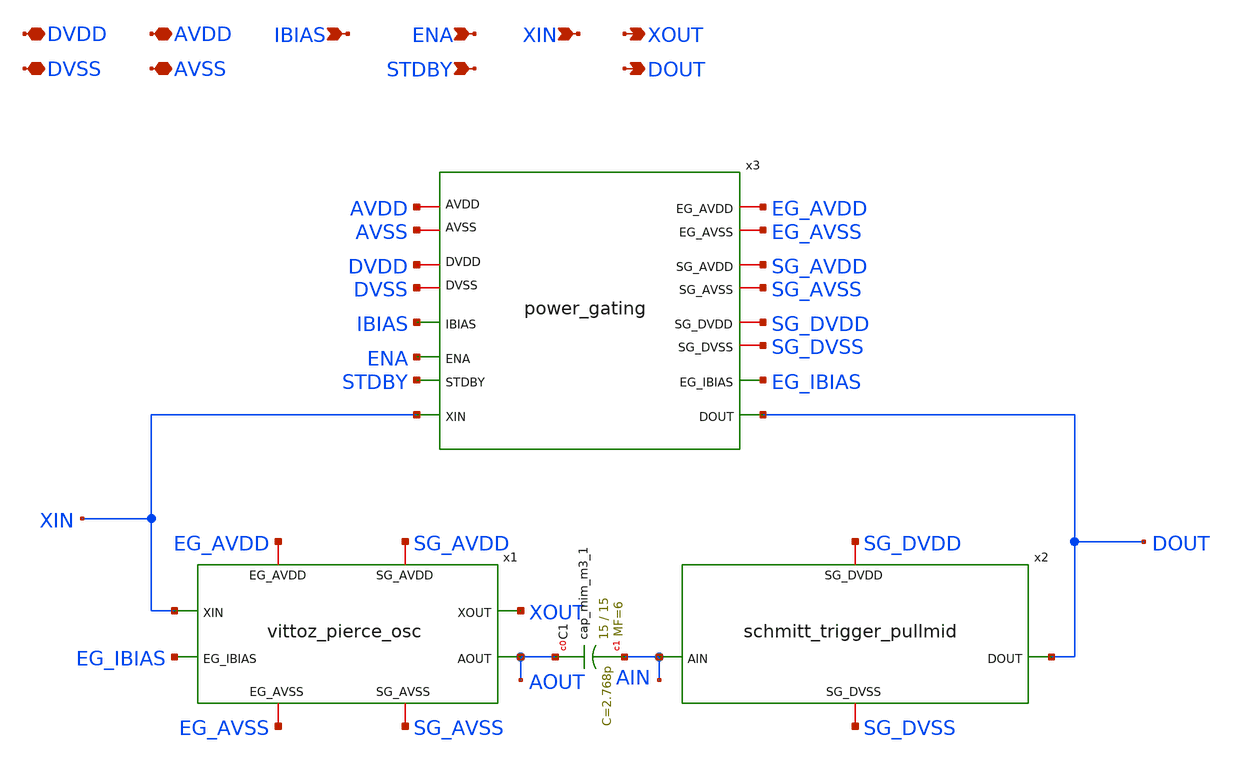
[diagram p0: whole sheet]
** sch_path: xschem/sky130_ht_ip__hsxo_cpz1.sch
**.subckt sky130_ht_ip__hsxo_cpz1 DVDD DVSS AVDD AVSS ENA STDBY XIN XOUT DOUT IBIAS
*.iopin DVDD
*.iopin DVSS
*.iopin AVDD
*.iopin AVSS
*.ipin ENA
*.ipin STDBY
*.ipin XIN
*.opin XOUT
*.opin DOUT
*.ipin IBIAS
x1 XOUT SG_AVDD EG_AVDD XIN EG_IBIAS AOUT SG_AVSS EG_AVSS vittoz_pierce_osc
x2 SG_DVDD AIN DOUT SG_DVSS schmitt_trigger_pullmid
XC1 AOUT AIN sky130_fd_pr__cap_mim_m3_1 W=15 L=15 MF=6 m=6
x3 DOUT SG_AVDD DVDD EG_IBIAS SG_DVDD AVDD IBIAS EG_AVDD ENA SG_DVSS SG_AVSS STDBY EG_AVSS AVSS DVSS
+ XIN power_gating
**.ends

* expanding   symbol:  vittoz_pierce_osc.sym # of pins=8
** sym_path: xschem/vittoz_pierce_osc.sym
** sch_path: xschem/vittoz_pierce_osc.sch
.subckt vittoz_pierce_osc XOUT SG_AVDD EG_AVDD XIN EG_IBIAS AOUT SG_AVSS EG_AVSS
*.iopin EG_AVDD
*.iopin EG_AVSS
*.iopin SG_AVDD
*.iopin SG_AVSS
*.ipin XIN
*.ipin EG_IBIAS
*.opin XOUT
*.opin AOUT
XM9 net6 PBIAS EG_AVDD EG_AVDD sky130_fd_pr__pfet_g5v0d10v5 L=0.5 W=1024 nf=32 ad='int((nf+1)/2) * W/nf * 0.29'
+ as='int((nf+2)/2) * W/nf * 0.29' pd='2*int((nf+1)/2) * (W/nf + 0.29)' ps='2*int((nf+2)/2) * (W/nf + 0.29)'
+ nrd='0.29 / W' nrs='0.29 / W' sa=0 sb=0 sd=0 mult=1 m=1
XM10 net7 PBIAS EG_AVDD EG_AVDD sky130_fd_pr__pfet_g5v0d10v5 L=0.5 W=128 nf=4 ad='int((nf+1)/2) * W/nf * 0.29'
+ as='int((nf+2)/2) * W/nf * 0.29' pd='2*int((nf+1)/2) * (W/nf + 0.29)' ps='2*int((nf+2)/2) * (W/nf + 0.29)'
+ nrd='0.29 / W' nrs='0.29 / W' sa=0 sb=0 sd=0 mult=1 m=1
XM11 PBIAS PBIAS EG_AVDD EG_AVDD sky130_fd_pr__pfet_g5v0d10v5 L=0.5 W=128 nf=4 ad='int((nf+1)/2) * W/nf * 0.29'
+ as='int((nf+2)/2) * W/nf * 0.29' pd='2*int((nf+1)/2) * (W/nf + 0.29)' ps='2*int((nf+2)/2) * (W/nf + 0.29)'
+ nrd='0.29 / W' nrs='0.29 / W' sa=0 sb=0 sd=0 mult=1 m=1
Vmeas3 net6 XOUT 0
.save i(vmeas3)
Vmeas4 net7 net1 0
.save i(vmeas4)
Vmeas2 PBIAS net3 0
.save i(vmeas2)
XM12 net1 net2 EG_AVSS EG_AVSS sky130_fd_pr__nfet_g5v0d10v5 L=0.5 W=128 nf=4 ad='int((nf+1)/2) * W/nf * 0.29'
+ as='int((nf+2)/2) * W/nf * 0.29' pd='2*int((nf+1)/2) * (W/nf + 0.29)' ps='2*int((nf+2)/2) * (W/nf + 0.29)'
+ nrd='0.29 / W' nrs='0.29 / W' sa=0 sb=0 sd=0 mult=1 m=1
XR1 net2 net1 EG_AVSS sky130_fd_pr__res_xhigh_po_0p35 L=7 mult=1 m=1
XC1 net1 EG_AVSS sky130_fd_pr__cap_mim_m3_1 W=2 L=2 MF=1 m=1
XC2 XIN net2 sky130_fd_pr__cap_mim_m3_1 W=15 L=15 MF=6 m=6
XC7 net2 EG_AVSS sky130_fd_pr__cap_mim_m3_1 W=15 L=15 MF=6 m=6
XM13 XOUT XIN EG_AVSS EG_AVSS sky130_fd_pr__nfet_g5v0d10v5 L=0.5 W=32 nf=8 ad='int((nf+1)/2) * W/nf * 0.29'
+ as='int((nf+2)/2) * W/nf * 0.29' pd='2*int((nf+1)/2) * (W/nf + 0.29)' ps='2*int((nf+2)/2) * (W/nf + 0.29)'
+ nrd='0.29 / W' nrs='0.29 / W' sa=0 sb=0 sd=0 mult=1 m=1
XM14 net3 net2 net5 EG_AVSS sky130_fd_pr__nfet_g5v0d10v5 L=0.5 W=1024 nf=32 ad='int((nf+1)/2) * W/nf * 0.29'
+ as='int((nf+2)/2) * W/nf * 0.29' pd='2*int((nf+1)/2) * (W/nf + 0.29)' ps='2*int((nf+2)/2) * (W/nf + 0.29)'
+ nrd='0.29 / W' nrs='0.29 / W' sa=0 sb=0 sd=0 mult=1 m=1
XM15 net5 net4 EG_AVSS EG_AVSS sky130_fd_pr__nfet_g5v0d10v5 L=0.5 W=128 nf=4 ad='int((nf+1)/2) * W/nf * 0.29'
+ as='int((nf+2)/2) * W/nf * 0.29' pd='2*int((nf+1)/2) * (W/nf + 0.29)' ps='2*int((nf+2)/2) * (W/nf + 0.29)'
+ nrd='0.29 / W' nrs='0.29 / W' sa=0 sb=0 sd=0 mult=1 m=1
XM16 net4 net4 EG_AVSS EG_AVSS sky130_fd_pr__nfet_g5v0d10v5 L=0.5 W=8 nf=1 ad='int((nf+1)/2) * W/nf * 0.29'
+ as='int((nf+2)/2) * W/nf * 0.29' pd='2*int((nf+1)/2) * (W/nf + 0.29)' ps='2*int((nf+2)/2) * (W/nf + 0.29)'
+ nrd='0.29 / W' nrs='0.29 / W' sa=0 sb=0 sd=0 mult=1 m=1
XR3 XIN XOUT EG_AVSS sky130_fd_pr__res_xhigh_po_0p35 L=2.8 mult=1 m=1
XM17 AOUT XIN SG_AVSS SG_AVSS sky130_fd_pr__nfet_g5v0d10v5 L=0.5 W=4 nf=1 ad='int((nf+1)/2) * W/nf * 0.29'
+ as='int((nf+2)/2) * W/nf * 0.29' pd='2*int((nf+1)/2) * (W/nf + 0.29)' ps='2*int((nf+2)/2) * (W/nf + 0.29)'
+ nrd='0.29 / W' nrs='0.29 / W' sa=0 sb=0 sd=0 mult=1 m=1
XM18 net8 PBIAS SG_AVDD SG_AVDD sky130_fd_pr__pfet_g5v0d10v5 L=0.5 W=128 nf=4 ad='int((nf+1)/2) * W/nf * 0.29'
+ as='int((nf+2)/2) * W/nf * 0.29' pd='2*int((nf+1)/2) * (W/nf + 0.29)' ps='2*int((nf+2)/2) * (W/nf + 0.29)'
+ nrd='0.29 / W' nrs='0.29 / W' sa=0 sb=0 sd=0 mult=1 m=1
Vmeas5 net8 AOUT 0
.save i(vmeas5)
XC8 AOUT SG_AVSS sky130_fd_pr__cap_mim_m3_1 W=2 L=2 MF=1 m=1
XC3 EG_AVDD EG_AVSS sky130_fd_pr__cap_mim_m3_1 W=15 L=15 MF=6 m=6
XC4 SG_AVDD SG_AVSS sky130_fd_pr__cap_mim_m3_1 W=15 L=15 MF=6 m=6
Vmeas1 EG_IBIAS net4 0
.save i(vmeas1)
.ends


* expanding   symbol:  schmitt_trigger_pullmid.sym # of pins=4
** sym_path: xschem/schmitt_trigger_pullmid.sym
** sch_path: xschem/schmitt_trigger_pullmid.sch
.subckt schmitt_trigger_pullmid SG_DVDD AIN DOUT SG_DVSS
*.iopin SG_DVDD
*.iopin SG_DVSS
*.ipin AIN
*.opin DOUT
XR3 net2 net1 SG_DVSS sky130_fd_pr__res_xhigh_po_0p35 L=128 mult=1 m=1
XM3 DOUT net2 DHT SG_DVDD sky130_fd_pr__pfet_01v8 L=0.3 W=1 nf=1 ad='int((1 + 1)/2) * 1 / 1 * 0.29' as='int((1 + 2)/2) * 1 / 1 * 0.29'
+ pd='2*int((1 + 1)/2) * (1 / 1 + 0.29)' ps='2*int((1 + 2)/2) * (1 / 1 + 0.29)' nrd='0.29 / 1 ' nrs='0.29 / 1 '
+ sa=0 sb=0 sd=0 mult=1 m=1
XM4 DOUT net2 DLT SG_DVSS sky130_fd_pr__nfet_01v8 L=0.2 W=1 nf=1 ad='int((nf+1)/2) * W/nf * 0.29' as='int((nf+2)/2) * W/nf * 0.29'
+ pd='2*int((nf+1)/2) * (W/nf + 0.29)' ps='2*int((nf+2)/2) * (W/nf + 0.29)' nrd='0.29 / W' nrs='0.29 / W'
+ sa=0 sb=0 sd=0 mult=1 m=1
XM5 DHT net2 SG_DVDD SG_DVDD sky130_fd_pr__pfet_01v8 L=0.3 W=1 nf=1 ad='int((1 + 1)/2) * 1 / 1 * 0.29'
+ as='int((1 + 2)/2) * 1 / 1 * 0.29' pd='2*int((1 + 1)/2) * (1 / 1 + 0.29)' ps='2*int((1 + 2)/2) * (1 / 1 + 0.29)'
+ nrd='0.29 / 1 ' nrs='0.29 / 1 ' sa=0 sb=0 sd=0 mult=1 m=1
XM6 DLT net2 SG_DVSS SG_DVSS sky130_fd_pr__nfet_01v8 L=0.2 W=1 nf=1 ad='int((nf+1)/2) * W/nf * 0.29'
+ as='int((nf+2)/2) * W/nf * 0.29' pd='2*int((nf+1)/2) * (W/nf + 0.29)' ps='2*int((nf+2)/2) * (W/nf + 0.29)'
+ nrd='0.29 / W' nrs='0.29 / W' sa=0 sb=0 sd=0 mult=1 m=1
XM7 SG_DVSS DOUT DHT SG_DVDD sky130_fd_pr__pfet_01v8 L=0.3 W=1 nf=1 ad='int((1 + 1)/2) * 1 / 1 * 0.29'
+ as='int((1 + 2)/2) * 1 / 1 * 0.29' pd='2*int((1 + 1)/2) * (1 / 1 + 0.29)' ps='2*int((1 + 2)/2) * (1 / 1 + 0.29)'
+ nrd='0.29 / 1 ' nrs='0.29 / 1 ' sa=0 sb=0 sd=0 mult=1 m=1
XM8 SG_DVDD DOUT DLT SG_DVSS sky130_fd_pr__nfet_01v8 L=0.2 W=1 nf=1 ad='int((nf+1)/2) * W/nf * 0.29'
+ as='int((nf+2)/2) * W/nf * 0.29' pd='2*int((nf+1)/2) * (W/nf + 0.29)' ps='2*int((nf+2)/2) * (W/nf + 0.29)'
+ nrd='0.29 / W' nrs='0.29 / W' sa=0 sb=0 sd=0 mult=1 m=1
XC4 SG_DVDD SG_DVSS sky130_fd_pr__cap_mim_m3_1 W=15 L=15 MF=6 m=6
XR1 net1 SG_DVDD SG_DVSS sky130_fd_pr__res_xhigh_po_0p35 L=16 mult=1 m=1
XR2 SG_DVSS net1 SG_DVSS sky130_fd_pr__res_xhigh_po_0p35 L=16 mult=1 m=1
Vmeas6 AIN net2 0
.save i(vmeas6)
.ends


* expanding   symbol:  /foss/designs/hsxo-cpz1/xschem/power_gating.sym # of pins=16
** sym_path: xschem/power_gating.sym
** sch_path: xschem/power_gating.sch
.subckt power_gating DOUT SG_AVDD DVDD EG_IBIAS SG_DVDD AVDD IBIAS EG_AVDD ENA SG_DVSS SG_AVSS STDBY
+ EG_AVSS AVSS DVSS XIN
*.iopin DVDD
*.iopin DVSS
*.iopin AVDD
*.iopin AVSS
*.ipin ENA
*.ipin STDBY
*.opin DOUT
*.ipin IBIAS
*.iopin EG_AVDD
*.iopin EG_AVSS
*.iopin SG_AVDD
*.iopin SG_AVSS
*.iopin SG_DVDD
*.iopin SG_DVSS
*.opin EG_IBIAS
*.ipin XIN
x3 AVDD ENA_B DVDD ENA ENA_H AVSS DVSS ENA_BH level_shifter
x4 AVDD STDBY_B DVDD STDBY STDBY_H AVSS DVSS STDBY_BH level_shifter
XM18 SG_DVSS STDBY_B DVSS DVSS sky130_fd_pr__nfet_01v8 L=0.15 W=8 nf=4 ad='int((nf+1)/2) * W/nf * 0.29'
+ as='int((nf+2)/2) * W/nf * 0.29' pd='2*int((nf+1)/2) * (W/nf + 0.29)' ps='2*int((nf+2)/2) * (W/nf + 0.29)'
+ nrd='0.29 / W' nrs='0.29 / W' sa=0 sb=0 sd=0 mult=1 m=1
XM21 EG_AVSS ENA_H AVSS AVSS sky130_fd_pr__nfet_g5v0d10v5 L=0.5 W=8 nf=4 ad='int((nf+1)/2) * W/nf * 0.29'
+ as='int((nf+2)/2) * W/nf * 0.29' pd='2*int((nf+1)/2) * (W/nf + 0.29)' ps='2*int((nf+2)/2) * (W/nf + 0.29)'
+ nrd='0.29 / W' nrs='0.29 / W' sa=0 sb=0 sd=0 mult=1 m=1
XM25 EG_AVDD ENA_BH AVDD AVDD sky130_fd_pr__pfet_g5v0d10v5 L=0.5 W=8 nf=4 ad='int((nf+1)/2) * W/nf * 0.29'
+ as='int((nf+2)/2) * W/nf * 0.29' pd='2*int((nf+1)/2) * (W/nf + 0.29)' ps='2*int((nf+2)/2) * (W/nf + 0.29)'
+ nrd='0.29 / W' nrs='0.29 / W' sa=0 sb=0 sd=0 mult=1 m=1
XM27 SG_DVDD STDBY DVDD DVDD sky130_fd_pr__pfet_01v8 L=0.15 W=8 nf=4 ad='int((4 + 1)/2) * 8 / 4 * 0.29'
+ as='int((4 + 2)/2) * 8 / 4 * 0.29' pd='2*int((4 + 1)/2) * (8 / 4 + 0.29)' ps='2*int((4 + 2)/2) * (8 / 4 + 0.29)'
+ nrd='0.29 / 8 ' nrs='0.29 / 8 ' sa=0 sb=0 sd=0 mult=1 m=1
XM1 SG_AVDD STDBY_H AVDD AVDD sky130_fd_pr__pfet_g5v0d10v5 L=0.5 W=8 nf=4 ad='int((nf+1)/2) * W/nf * 0.29'
+ as='int((nf+2)/2) * W/nf * 0.29' pd='2*int((nf+1)/2) * (W/nf + 0.29)' ps='2*int((nf+2)/2) * (W/nf + 0.29)'
+ nrd='0.29 / W' nrs='0.29 / W' sa=0 sb=0 sd=0 mult=1 m=1
XM2 EG_IBIAS ENA_BH IBIAS AVDD sky130_fd_pr__pfet_g5v0d10v5 L=0.5 W=8 nf=4 ad='int((nf+1)/2) * W/nf * 0.29'
+ as='int((nf+2)/2) * W/nf * 0.29' pd='2*int((nf+1)/2) * (W/nf + 0.29)' ps='2*int((nf+2)/2) * (W/nf + 0.29)'
+ nrd='0.29 / W' nrs='0.29 / W' sa=0 sb=0 sd=0 mult=1 m=1
XM3 SG_AVSS STDBY_BH AVSS AVSS sky130_fd_pr__nfet_g5v0d10v5 L=0.5 W=8 nf=4 ad='int((nf+1)/2) * W/nf * 0.29'
+ as='int((nf+2)/2) * W/nf * 0.29' pd='2*int((nf+1)/2) * (W/nf + 0.29)' ps='2*int((nf+2)/2) * (W/nf + 0.29)'
+ nrd='0.29 / W' nrs='0.29 / W' sa=0 sb=0 sd=0 mult=1 m=1
XM4 DOUT STDBY DVSS DVSS sky130_fd_pr__nfet_01v8 L=0.15 W=8 nf=4 ad='int((nf+1)/2) * W/nf * 0.29' as='int((nf+2)/2) * W/nf * 0.29'
+ pd='2*int((nf+1)/2) * (W/nf + 0.29)' ps='2*int((nf+2)/2) * (W/nf + 0.29)' nrd='0.29 / W' nrs='0.29 / W'
+ sa=0 sb=0 sd=0 mult=1 m=1
XC3 AVDD AVSS sky130_fd_pr__cap_mim_m3_1 W=15 L=15 MF=6 m=6
XC4 DVDD DVSS sky130_fd_pr__cap_mim_m3_1 W=15 L=15 MF=6 m=6
XD1 XIN AVDD sky130_fd_pr__diode_pd2nw_05v5 area=2e11 pj=1.8e6
XD2 AVSS XIN sky130_fd_pr__diode_pw2nd_05v5 area=2e11 pj=1.8e6
.ends


* expanding   symbol:  level_shifter.sym # of pins=8
** sym_path: xschem/level_shifter.sym
** sch_path: xschem/level_shifter.sch
.subckt level_shifter AVDD LO_B DVDD LO HI AVSS DVSS HI_B
*.iopin DVDD
*.iopin DVSS
*.iopin AVDD
*.iopin AVSS
*.ipin LO
*.opin LO_B
*.opin HI
*.opin HI_B
XM18 LO_B LO DVSS DVSS sky130_fd_pr__nfet_01v8 L=0.15 W=1 nf=1 ad='int((nf+1)/2) * W/nf * 0.29' as='int((nf+2)/2) * W/nf * 0.29'
+ pd='2*int((nf+1)/2) * (W/nf + 0.29)' ps='2*int((nf+2)/2) * (W/nf + 0.29)' nrd='0.29 / W' nrs='0.29 / W'
+ sa=0 sb=0 sd=0 mult=1 m=1
XM21 HI_B LO AVSS AVSS sky130_fd_pr__nfet_g5v0d10v5 L=0.5 W=1 nf=1 ad='int((nf+1)/2) * W/nf * 0.29' as='int((nf+2)/2) * W/nf * 0.29'
+ pd='2*int((nf+1)/2) * (W/nf + 0.29)' ps='2*int((nf+2)/2) * (W/nf + 0.29)' nrd='0.29 / W' nrs='0.29 / W'
+ sa=0 sb=0 sd=0 mult=1 m=1
XM25 HI_B HI AVDD AVDD sky130_fd_pr__pfet_g5v0d10v5 L=0.5 W=1 nf=1 ad='int((nf+1)/2) * W/nf * 0.29' as='int((nf+2)/2) * W/nf * 0.29'
+ pd='2*int((nf+1)/2) * (W/nf + 0.29)' ps='2*int((nf+2)/2) * (W/nf + 0.29)' nrd='0.29 / W' nrs='0.29 / W'
+ sa=0 sb=0 sd=0 mult=1 m=1
XM27 LO_B LO DVDD DVDD sky130_fd_pr__pfet_01v8 L=0.15 W=1 nf=1 ad='int((1 + 1)/2) * 1 / 1 * 0.29' as='int((1 + 2)/2) * 1 / 1 * 0.29'
+ pd='2*int((1 + 1)/2) * (1 / 1 + 0.29)' ps='2*int((1 + 2)/2) * (1 / 1 + 0.29)' nrd='0.29 / 1 ' nrs='0.29 / 1 '
+ sa=0 sb=0 sd=0 mult=1 m=1
XM1 HI HI_B AVDD AVDD sky130_fd_pr__pfet_g5v0d10v5 L=0.5 W=1 nf=1 ad='int((nf+1)/2) * W/nf * 0.29' as='int((nf+2)/2) * W/nf * 0.29'
+ pd='2*int((nf+1)/2) * (W/nf + 0.29)' ps='2*int((nf+2)/2) * (W/nf + 0.29)' nrd='0.29 / W' nrs='0.29 / W'
+ sa=0 sb=0 sd=0 mult=1 m=1
XM2 HI LO_B AVSS AVSS sky130_fd_pr__nfet_g5v0d10v5 L=0.5 W=1 nf=1 ad='int((nf+1)/2) * W/nf * 0.29' as='int((nf+2)/2) * W/nf * 0.29'
+ pd='2*int((nf+1)/2) * (W/nf + 0.29)' ps='2*int((nf+2)/2) * (W/nf + 0.29)' nrd='0.29 / W' nrs='0.29 / W'
+ sa=0 sb=0 sd=0 mult=1 m=1
.ends

.end
